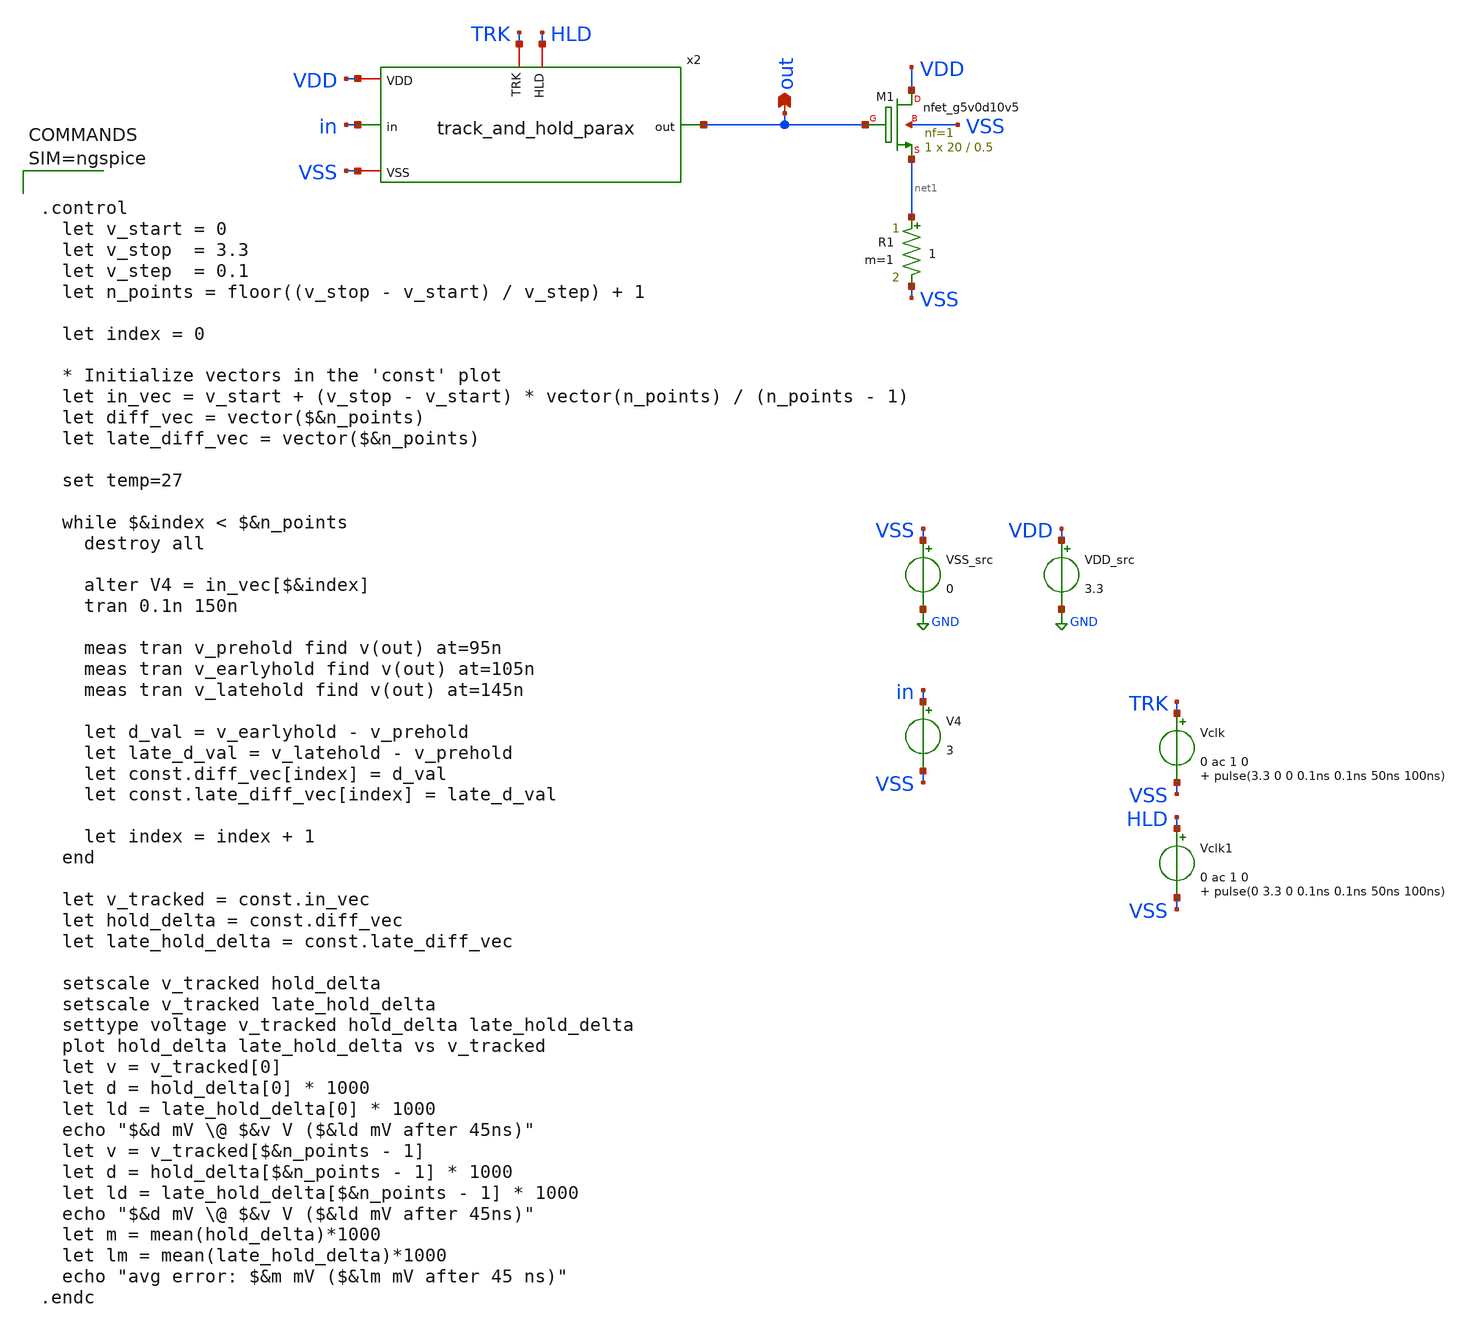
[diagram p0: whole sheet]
** sch_path: xschem/track_and_hold/hold_testbench.sch
**.subckt hold_testbench out
*.opin out
VDD_src VDD GND 3.3
VSS_src VSS GND 0
V4 in VSS 3
XM1 VDD out net1 VSS sky130_fd_pr__nfet_g5v0d10v5 L=0.5 W=20 nf=1 ad='int((nf+1)/2) * W/nf * 0.29' as='int((nf+2)/2) * W/nf * 0.29'
+ pd='2*int((nf+1)/2) * (W/nf + 0.29)' ps='2*int((nf+2)/2) * (W/nf + 0.29)' nrd='0.29 / W' nrs='0.29 / W'
+ sa=0 sb=0 sd=0 mult=1 m=1
R1 net1 VSS 1 m=1
Vclk TRK VSS 0 ac 1 0 pulse(3.3 0 0 0.1ns 0.1ns 50ns 100ns)
Vclk1 HLD VSS 0 ac 1 0 pulse(0 3.3 0 0.1ns 0.1ns 50ns 100ns)
x2 HLD TRK VDD VSS out in track_and_hold_parax
**** begin user architecture code

** opencircuitdesign pdks install
.lib $::SKYWATER_MODELS/sky130.lib.spice ss





.control
  let v_start = 0
  let v_stop  = 3.3
  let v_step  = 0.1
  let n_points = floor((v_stop - v_start) / v_step) + 1

  let index = 0

  * Initialize vectors in the 'const' plot
  let in_vec = v_start + (v_stop - v_start) * vector(n_points) / (n_points - 1)
  let diff_vec = vector($&n_points)
  let late_diff_vec = vector($&n_points)

  set temp=27

  while $&index < $&n_points
    destroy all

    alter V4 = in_vec[$&index]
    tran 0.1n 150n

    meas tran v_prehold find v(out) at=95n
    meas tran v_earlyhold find v(out) at=105n
    meas tran v_latehold find v(out) at=145n

    let d_val = v_earlyhold - v_prehold
    let late_d_val = v_latehold - v_prehold
    let const.diff_vec[index] = d_val
    let const.late_diff_vec[index] = late_d_val

    let index = index + 1
  end

  let v_tracked = const.in_vec
  let hold_delta = const.diff_vec
  let late_hold_delta = const.late_diff_vec

  setscale v_tracked hold_delta
  setscale v_tracked late_hold_delta
  settype voltage v_tracked hold_delta late_hold_delta
  plot hold_delta late_hold_delta vs v_tracked
  let v = v_tracked[0]
  let d = hold_delta[0] * 1000
  let ld = late_hold_delta[0] * 1000
  echo "$&d mV \@ $&v V ($&ld mV after 45ns)"
  let v = v_tracked[$&n_points - 1]
  let d = hold_delta[$&n_points - 1] * 1000
  let ld = late_hold_delta[$&n_points - 1] * 1000
  echo "$&d mV \@ $&v V ($&ld mV after 45ns)"
  let m = mean(hold_delta)*1000
  let lm = mean(late_hold_delta)*1000
  echo "avg error: $&m mV ($&lm mV after 45 ns)"
.endc



**** end user architecture code
**.ends

* expanding   symbol:  track_and_hold_parax.sym # of pins=6
** sym_path: xschem/track_and_hold.sym
.include [file normalize ../../mag/track_and_hold.sim.spice]
.GLOBAL GND
.end
